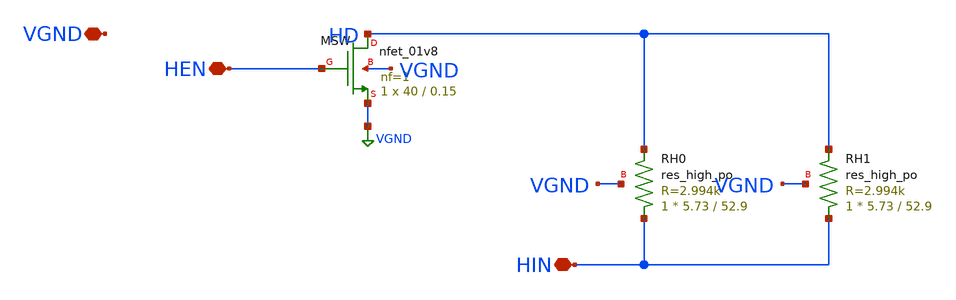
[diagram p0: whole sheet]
** sch_path: cells/ELAD1_HEATER/schematic/ELAD1_HEATER.sch
**.subckt ELAD1_HEATER HIN HEN VGND
*.iopin HIN
*.iopin HEN
*.iopin VGND
XRH0 HIN HD VGND sky130_fd_pr__res_high_po W=5.73 L=52.9 mult=1 m=1
XRH1 HIN HD VGND sky130_fd_pr__res_high_po W=5.73 L=52.9 mult=1 m=1
XMSW HD HEN VGND VGND sky130_fd_pr__nfet_01v8 L=0.15 W=40 nf=1 ad='int((1 + 1)/2) * 40 / 1 * 0.29' as='int((1 + 2)/2) * 40 / 1 * 0.29'
+ pd='2*int((1 + 1)/2) * (40 / 1 + 0.29)' ps='2*int((1 + 2)/2) * (40 / 1 + 0.29)' nrd='0.29 / 40 ' nrs='0.29 / 40 '
+ sa=0 sb=0 sd=0 mult=1 m=1
**.ends
.GLOBAL VGND
.end
